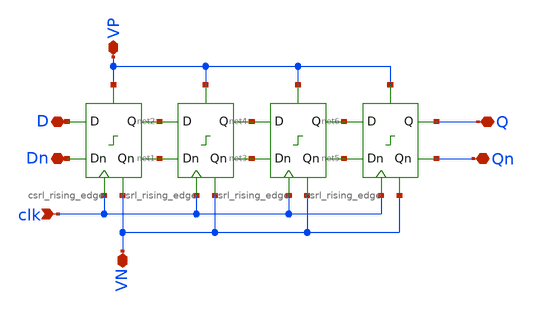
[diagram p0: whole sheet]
** sch_path: lib/digital/schematic/shift_register_x4_rising.sch
**.subckt shift_register_x4_rising clk Q Qn D Dn VP VN
*.ipin clk
*.iopin Q
*.iopin Qn
*.iopin D
*.iopin Dn
*.iopin VP
*.iopin VN
X1 D Dn net1 net2 VN clk VP csrl_rising_edge
X2 net2 net1 net3 net4 VN clk VP csrl_rising_edge
X3 net4 net3 net5 net6 VN clk VP csrl_rising_edge
X4 net6 net5 Qn Q VN clk VP csrl_rising_edge
**.ends
.end
